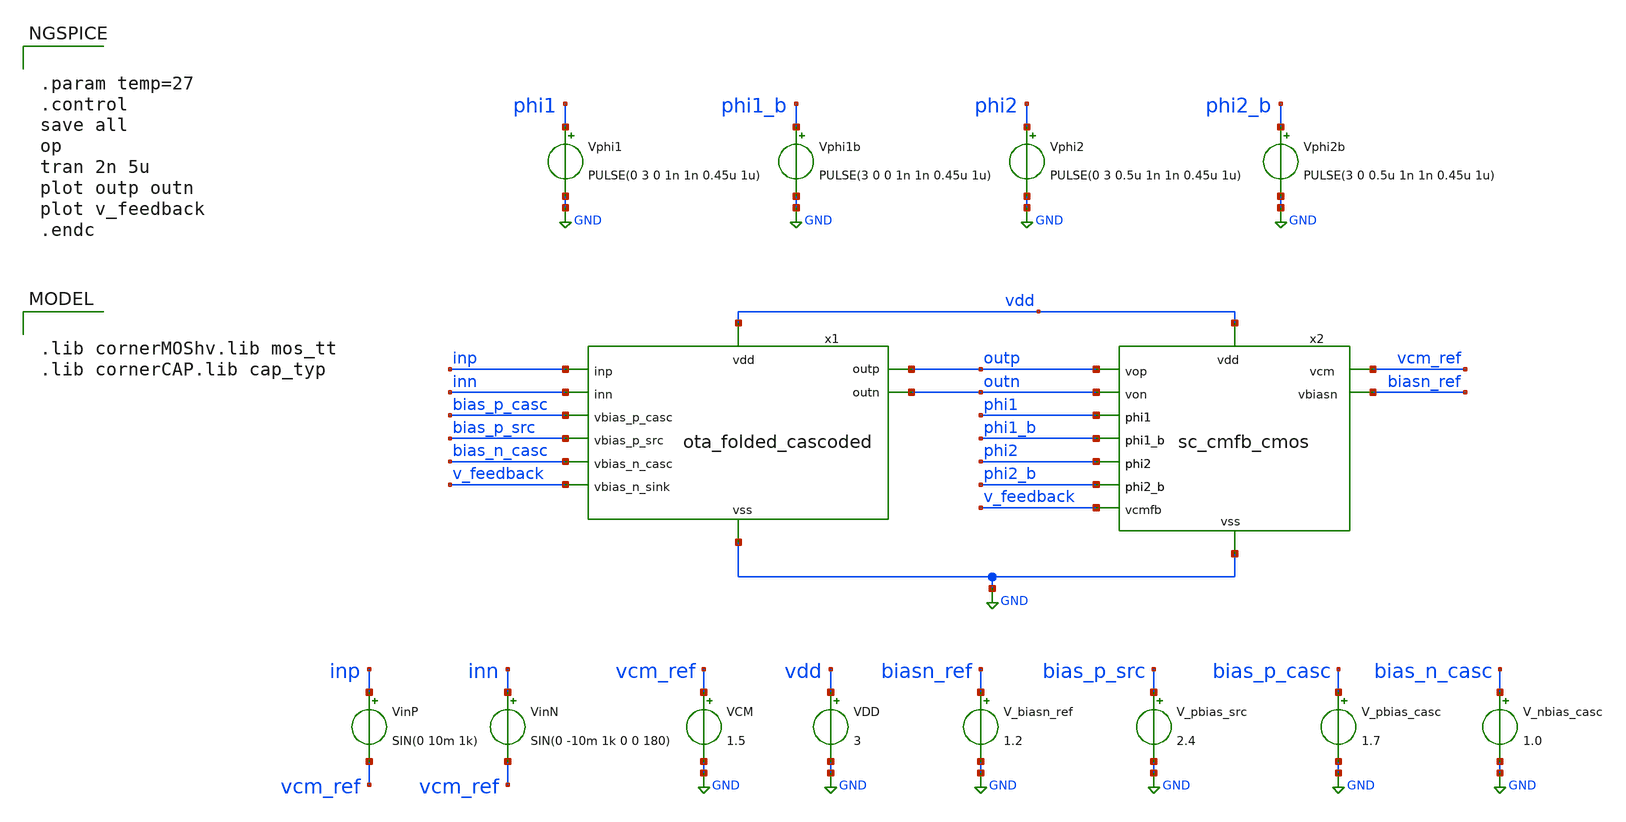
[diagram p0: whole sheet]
** sch_path: 3_real_circuits/ota_sc_cmfb_tb.sch
**.subckt ota_sc_cmfb_tb
VCM vcm_ref GND 1.5
VinP inp vcm_ref SIN(0 10m 1k)
VinN inn vcm_ref SIN(0 -10m 1k 0 0 180)
x1 inp inn outp GND outn bias_p_casc bias_p_src bias_n_casc v_feedback vdd ota_folded_cascoded
x2 outp outn vcm_ref phi1 phi1_b phi2 phi2_b biasn_ref GND vdd v_feedback sc_cmfb_cmos
Vphi1 phi1 GND PULSE(0 3 0 1n 1n 0.45u 1u)
V_biasn_ref biasn_ref GND 1.2
VDD vdd GND 3
V_pbias_src bias_p_src GND 2.4
V_pbias_casc bias_p_casc GND 1.7
V_nbias_casc bias_n_casc GND 1.0
Vphi1b phi1_b GND PULSE(3 0 0 1n 1n 0.45u 1u)
Vphi2 phi2 GND PULSE(0 3 0.5u 1n 1n 0.45u 1u)
Vphi2b phi2_b GND PULSE(3 0 0.5u 1n 1n 0.45u 1u)
**** begin user architecture code


.param temp=27
.control
save all
op
tran 2n 5u
plot outp outn
plot v_feedback
.endc



.lib cornerMOShv.lib mos_tt
.lib cornerCAP.lib cap_typ

**** end user architecture code
**.ends

* expanding   symbol:  ota_folded_cascoded.sym # of pins=12
** sym_path: 3_real_circuits/ota_folded_cascoded.sym
** sch_path: 3_real_circuits/ota_folded_cascoded.sch
.subckt ota_folded_cascoded inp inn outp vss outn vbias_p_casc vbias_p_src vbias_n_casc vbias_n_sink
+ vdd
*.ipin inp
*.ipin inn
*.iopin vss
*.ipin vdd
*.opin outn
*.opin outp
*.ipin vbias_n_casc
*.ipin vbias_p_casc
*.ipin vbias_p_src
*.ipin vbias_n_sink
XM1 net5 inp net1 vss sg13_hv_nmos w=6.2u l=1u ng=1 m=1 mm_ok=1
XM10 net5 vbias_p_src vdd vdd sg13_hv_pmos w=7.05u l=1u ng=1 m=1 mm_ok=1
XM8 outn vbias_p_casc net5 vdd sg13_hv_pmos w=4.6u l=0.4u ng=1 m=1 mm_ok=1
XM11 net4 vbias_p_src vdd vdd sg13_hv_pmos w=7.05u l=1u ng=1 m=1 mm_ok=1
XM9 outp vbias_p_casc net4 vdd sg13_hv_pmos w=4.6u l=0.4u ng=1 m=1 mm_ok=1
XM7 outp vbias_n_casc net3 vss sg13_hv_nmos w=1u l=0.45u ng=1 m=1 mm_ok=1
XM5 net3 vbias_n_sink vss vss sg13_hv_nmos w=1.13u l=1u ng=1 m=1 mm_ok=1
XM4 net2 vbias_n_sink vss vss sg13_hv_nmos w=1.13u l=1u ng=1 m=1 mm_ok=1
XM6 outn vbias_n_casc net2 vss sg13_hv_nmos w=1u l=0.45u ng=1 m=1 mm_ok=1
XM2 net4 inn net1 vss sg13_hv_nmos w=6.2u l=1u ng=1 m=1 mm_ok=1
XM3 net1 vbias_n_sink vss vss sg13_hv_nmos w=3.25u l=1.5u ng=1 m=1 mm_ok=1
.ends


* expanding   symbol:  sc_cmfb_cmos.sym # of pins=11
** sym_path: 3_real_circuits/sc_cmfb_cmos.sym
** sch_path: 3_real_circuits/sc_cmfb_cmos.sch
.subckt sc_cmfb_cmos vop von vcm phi1 phi1_b phi2 phi2_b vbiasn vss vdd vcmfb
*.ipin von
*.ipin vop
*.ipin phi2_b
*.ipin phi2
*.ipin phi1_b
*.ipin phi1
*.ipin vdd
*.iopin vss
*.iopin vbiasn
*.iopin vcm
*.iopin vcmfb
XC1 net1 net3 cap_cmim w=10.0e-6 l=10.0e-6 m=1 mm_ok=1
XC3 von vcmfb cap_cmim w=10.0e-6 l=10.0e-6 m=1 mm_ok=1
XC4 vop vcmfb cap_cmim w=10.0e-6 l=10.0e-6 m=1 mm_ok=1
XC2 net2 net4 cap_cmim w=10.0e-6 l=10.0e-6 m=1 mm_ok=1
XM2 net1 phi1_b vcm vdd sg13_hv_pmos w=4u l=0.45u ng=1 m=1 mm_ok=1
XM1 net1 phi1 vcm vss sg13_hv_nmos w=2u l=0.45u ng=1 m=1 mm_ok=1
XM3 von phi2_b net1 vdd sg13_hv_pmos w=4u l=0.45u ng=1 m=1 mm_ok=1
XM4 von phi2 net1 vss sg13_hv_nmos w=2u l=0.45u ng=1 m=1 mm_ok=1
XM5 net2 phi2_b vop vdd sg13_hv_pmos w=4u l=0.45u ng=1 m=1 mm_ok=1
XM6 net2 phi2 vop vss sg13_hv_nmos w=2u l=0.45u ng=1 m=1 mm_ok=1
XM7 vcm phi1_b net2 vdd sg13_hv_pmos w=4u l=0.45u ng=1 m=1 mm_ok=1
XM8 vcm phi1 net2 vss sg13_hv_nmos w=2u l=0.45u ng=1 m=1 mm_ok=1
XM9 net3 phi1_b vbiasn vdd sg13_hv_pmos w=4u l=0.45u ng=1 m=1 mm_ok=1
XM10 net3 phi1 vbiasn vss sg13_hv_nmos w=2u l=0.45u ng=1 m=1 mm_ok=1
XM11 vcmfb phi2_b net3 vdd sg13_hv_pmos w=4u l=0.45u ng=1 m=1 mm_ok=1
XM12 vcmfb phi2 net3 vss sg13_hv_nmos w=2u l=0.45u ng=1 m=1 mm_ok=1
XM13 net4 phi2_b vcmfb vdd sg13_hv_pmos w=4u l=0.45u ng=1 m=1 mm_ok=1
XM14 net4 phi2 vcmfb vss sg13_hv_nmos w=2u l=0.45u ng=1 m=1 mm_ok=1
XM15 vbiasn phi1_b net4 vdd sg13_hv_pmos w=4u l=0.45u ng=1 m=1 mm_ok=1
XM16 vbiasn phi1 net4 vss sg13_hv_nmos w=2u l=0.45u ng=1 m=1 mm_ok=1
.ends

.GLOBAL GND
.end
